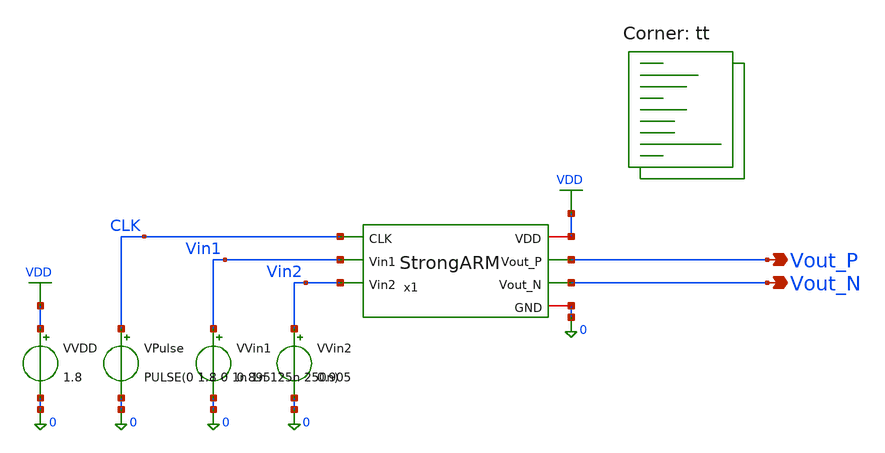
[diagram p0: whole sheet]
** sch_path: blocks/03_StrongARM/sim/tb_StrongARM_Power.sch
**.subckt tb_StrongARM_Power Vout_P Vout_N
*.opin Vout_P
*.opin Vout_N
x1 VDD CLK Vout_P Vout_N Vin1 Vin2 0 StrongARM
VVDD VDD 0 1.8
VVin1 Vin1 0 0.895
VVin2 Vin2 0 0.905
VPulse CLK 0 PULSE(0 1.8 0 1n 1n 125n 250n)
**** begin user architecture code



.control
save all

* ==========================================
* BLOCK 3 - STRONGARM COMPARATOR
* TEST 7A + 7C: POWER AND OUTPUT LOADING
* TECHNOLOGY: SKY130
* VDD = 1.8 V
* CLOCK = 4 MHz
* CORNER = tt
* VCM = 0.9 V
* Vin1 = 0.895 V
* Vin2 = 0.905 V
* Expected falling output: Vout_N
* ==========================================

echo ==========================================
echo STRONGARM POWER AND LOADING TEST
echo ==========================================

* Transient simulation
tran 0.2n 2.5u

* ==========================================
* A. DECISION DELAY
* Ninth clock rising edge at approximately 2us
* ==========================================

meas tran t_decision TRIG v(clk) VAL=0.9 RISE=9 TARG v(vout_n) VAL=0.9 FALL=9

* ==========================================
* B. OUTPUT LOGIC VERIFICATION
* ==========================================

meas tran vp_eval FIND v(vout_p) AT=2.01u
meas tran vn_eval FIND v(vout_n) AT=2.01u

meas tran vp_reset FIND v(vout_p) AT=2.20u
meas tran vn_reset FIND v(vout_n) AT=2.20u

* ==========================================
* C. AVERAGE SUPPLY CURRENT
* Ignore the first 500ns
* ==========================================

meas tran ivdd_avg AVG i(VVDD) FROM=500n TO=2.5u

* ==========================================
* D. POWER AND ENERGY
* ==========================================

let p_avg = -1.8 * ivdd_avg
let e_decision = p_avg / 4e6

let power_uW = p_avg * 1e6
let energy_pJ = e_decision * 1e12
let delay_ns = t_decision * 1e9

echo ==========================================
echo TEST 7A - POWER RESULTS
echo ==========================================

print ivdd_avg
print power_uW
print energy_pJ

echo ==========================================
echo TEST 7C - TIMING RESULTS
echo ==========================================

print delay_ns

echo ==========================================
echo TEST 7C - OUTPUT VOLTAGE LIMITS
echo ==========================================

meas tran vp_max MAX v(vout_p) FROM=500n TO=2.5u
meas tran vp_min MIN v(vout_p) FROM=500n TO=2.5u

meas tran vn_max MAX v(vout_n) FROM=500n TO=2.5u
meas tran vn_min MIN v(vout_n) FROM=500n TO=2.5u

echo ==========================================
echo TEST 7C - HIGH OUTPUT DROOP
echo ==========================================

meas tran vp_droop_min MIN v(vout_p) FROM=2u TO=2.01u

echo ==========================================
echo ALL MEASUREMENTS COMPLETED
echo ==========================================

.endc

.lib $::SKYWATER_MODELS/sky130.lib.spice tt
**** end user architecture code
**.ends

* expanding   symbol:  blocks/03_StrongARM/xschem/StrongARM.sym # of pins=7
** sym_path: blocks/03_StrongARM/xschem/StrongARM.sym
** sch_path: blocks/03_StrongARM/xschem/StrongARM.sch
.subckt StrongARM VDD CLK Vout_P Vout_N Vin1 Vin2 GND
*.iopin VDD
*.iopin GND
*.ipin Vin1
*.ipin Vin2
*.ipin CLK
*.opin Vout_P
*.opin Vout_N
XS1 P CLK VDD VDD sky130_fd_pr__pfet_01v8 L=0.15 W=1.5 nf=1 ad='int((1 + 1)/2) * 1.5 / 1 * 0.29' as='int((1 + 2)/2) * 1.5 / 1 * 0.29'
+ pd='2*int((1 + 1)/2) * (1.5 / 1 + 0.29)' ps='2*int((1 + 2)/2) * (1.5 / 1 + 0.29)' nrd='0.29 / 1.5 ' nrs='0.29 / 1.5 '
+ sa=0 sb=0 sd=0 mult=1 m=1
XS3 Vout_P CLK VDD VDD sky130_fd_pr__pfet_01v8 L=0.15 W=1.5 nf=1 ad='int((1 + 1)/2) * 1.5 / 1 * 0.29'
+ as='int((1 + 2)/2) * 1.5 / 1 * 0.29' pd='2*int((1 + 1)/2) * (1.5 / 1 + 0.29)' ps='2*int((1 + 2)/2) * (1.5 / 1 + 0.29)'
+ nrd='0.29 / 1.5 ' nrs='0.29 / 1.5 ' sa=0 sb=0 sd=0 mult=1 m=1
XM5 Vout_P Vout_N VDD VDD sky130_fd_pr__pfet_01v8 L=0.3 W=5 nf=1 ad='int((1 + 1)/2) * 5 / 1 * 0.29' as='int((1 + 2)/2) * 5 / 1 * 0.29'
+ pd='2*int((1 + 1)/2) * (5 / 1 + 0.29)' ps='2*int((1 + 2)/2) * (5 / 1 + 0.29)' nrd='0.29 / 5 ' nrs='0.29 / 5 '
+ sa=0 sb=0 sd=0 mult=1 m=1
XM6 Vout_N Vout_P VDD VDD sky130_fd_pr__pfet_01v8 L=0.3 W=5 nf=1 ad='int((1 + 1)/2) * 5 / 1 * 0.29' as='int((1 + 2)/2) * 5 / 1 * 0.29'
+ pd='2*int((1 + 1)/2) * (5 / 1 + 0.29)' ps='2*int((1 + 2)/2) * (5 / 1 + 0.29)' nrd='0.29 / 5 ' nrs='0.29 / 5 '
+ sa=0 sb=0 sd=0 mult=1 m=1
XS4 Vout_N CLK VDD VDD sky130_fd_pr__pfet_01v8 L=0.15 W=1.5 nf=1 ad='int((1 + 1)/2) * 1.5 / 1 * 0.29'
+ as='int((1 + 2)/2) * 1.5 / 1 * 0.29' pd='2*int((1 + 1)/2) * (1.5 / 1 + 0.29)' ps='2*int((1 + 2)/2) * (1.5 / 1 + 0.29)'
+ nrd='0.29 / 1.5 ' nrs='0.29 / 1.5 ' sa=0 sb=0 sd=0 mult=1 m=1
XS2 Q CLK VDD VDD sky130_fd_pr__pfet_01v8 L=0.15 W=1.5 nf=1 ad='int((1 + 1)/2) * 1.5 / 1 * 0.29' as='int((1 + 2)/2) * 1.5 / 1 * 0.29'
+ pd='2*int((1 + 1)/2) * (1.5 / 1 + 0.29)' ps='2*int((1 + 2)/2) * (1.5 / 1 + 0.29)' nrd='0.29 / 1.5 ' nrs='0.29 / 1.5 '
+ sa=0 sb=0 sd=0 mult=1 m=1
XM3 Vout_P Vout_N P GND sky130_fd_pr__nfet_01v8 L=0.3 W=2 nf=1 ad='int((1 + 1)/2) * 2 / 1 * 0.29' as='int((1 + 2)/2) * 2 / 1 * 0.29'
+ pd='2*int((1 + 1)/2) * (2 / 1 + 0.29)' ps='2*int((1 + 2)/2) * (2 / 1 + 0.29)' nrd='0.29 / 2 ' nrs='0.29 / 2 '
+ sa=0 sb=0 sd=0 mult=1 m=1
XM4 Vout_N Vout_P Q GND sky130_fd_pr__nfet_01v8 L=0.3 W=2 nf=1 ad='int((1 + 1)/2) * 2 / 1 * 0.29' as='int((1 + 2)/2) * 2 / 1 * 0.29'
+ pd='2*int((1 + 1)/2) * (2 / 1 + 0.29)' ps='2*int((1 + 2)/2) * (2 / 1 + 0.29)' nrd='0.29 / 2 ' nrs='0.29 / 2 '
+ sa=0 sb=0 sd=0 mult=1 m=1
XM1 P Vin1 TAIL GND sky130_fd_pr__nfet_01v8 L=0.5 W=10 nf=1 ad='int((1 + 1)/2) * 10 / 1 * 0.29' as='int((1 + 2)/2) * 10 / 1 * 0.29'
+ pd='2*int((1 + 1)/2) * (10 / 1 + 0.29)' ps='2*int((1 + 2)/2) * (10 / 1 + 0.29)' nrd='0.29 / 10 ' nrs='0.29 / 10 '
+ sa=0 sb=0 sd=0 mult=1 m=1
XM2 Q Vin2 TAIL GND sky130_fd_pr__nfet_01v8 L=0.5 W=10 nf=1 ad='int((1 + 1)/2) * 10 / 1 * 0.29' as='int((1 + 2)/2) * 10 / 1 * 0.29'
+ pd='2*int((1 + 1)/2) * (10 / 1 + 0.29)' ps='2*int((1 + 2)/2) * (10 / 1 + 0.29)' nrd='0.29 / 10 ' nrs='0.29 / 10 '
+ sa=0 sb=0 sd=0 mult=1 m=1
XM7 TAIL CLK GND GND sky130_fd_pr__nfet_01v8 L=0.3 W=1 nf=1 ad='int((1 + 1)/2) * 1 / 1 * 0.29' as='int((1 + 2)/2) * 1 / 1 * 0.29'
+ pd='2*int((1 + 1)/2) * (1 / 1 + 0.29)' ps='2*int((1 + 2)/2) * (1 / 1 + 0.29)' nrd='0.29 / 1 ' nrs='0.29 / 1 '
+ sa=0 sb=0 sd=0 mult=1 m=1
.ends

.GLOBAL VDD
.end
